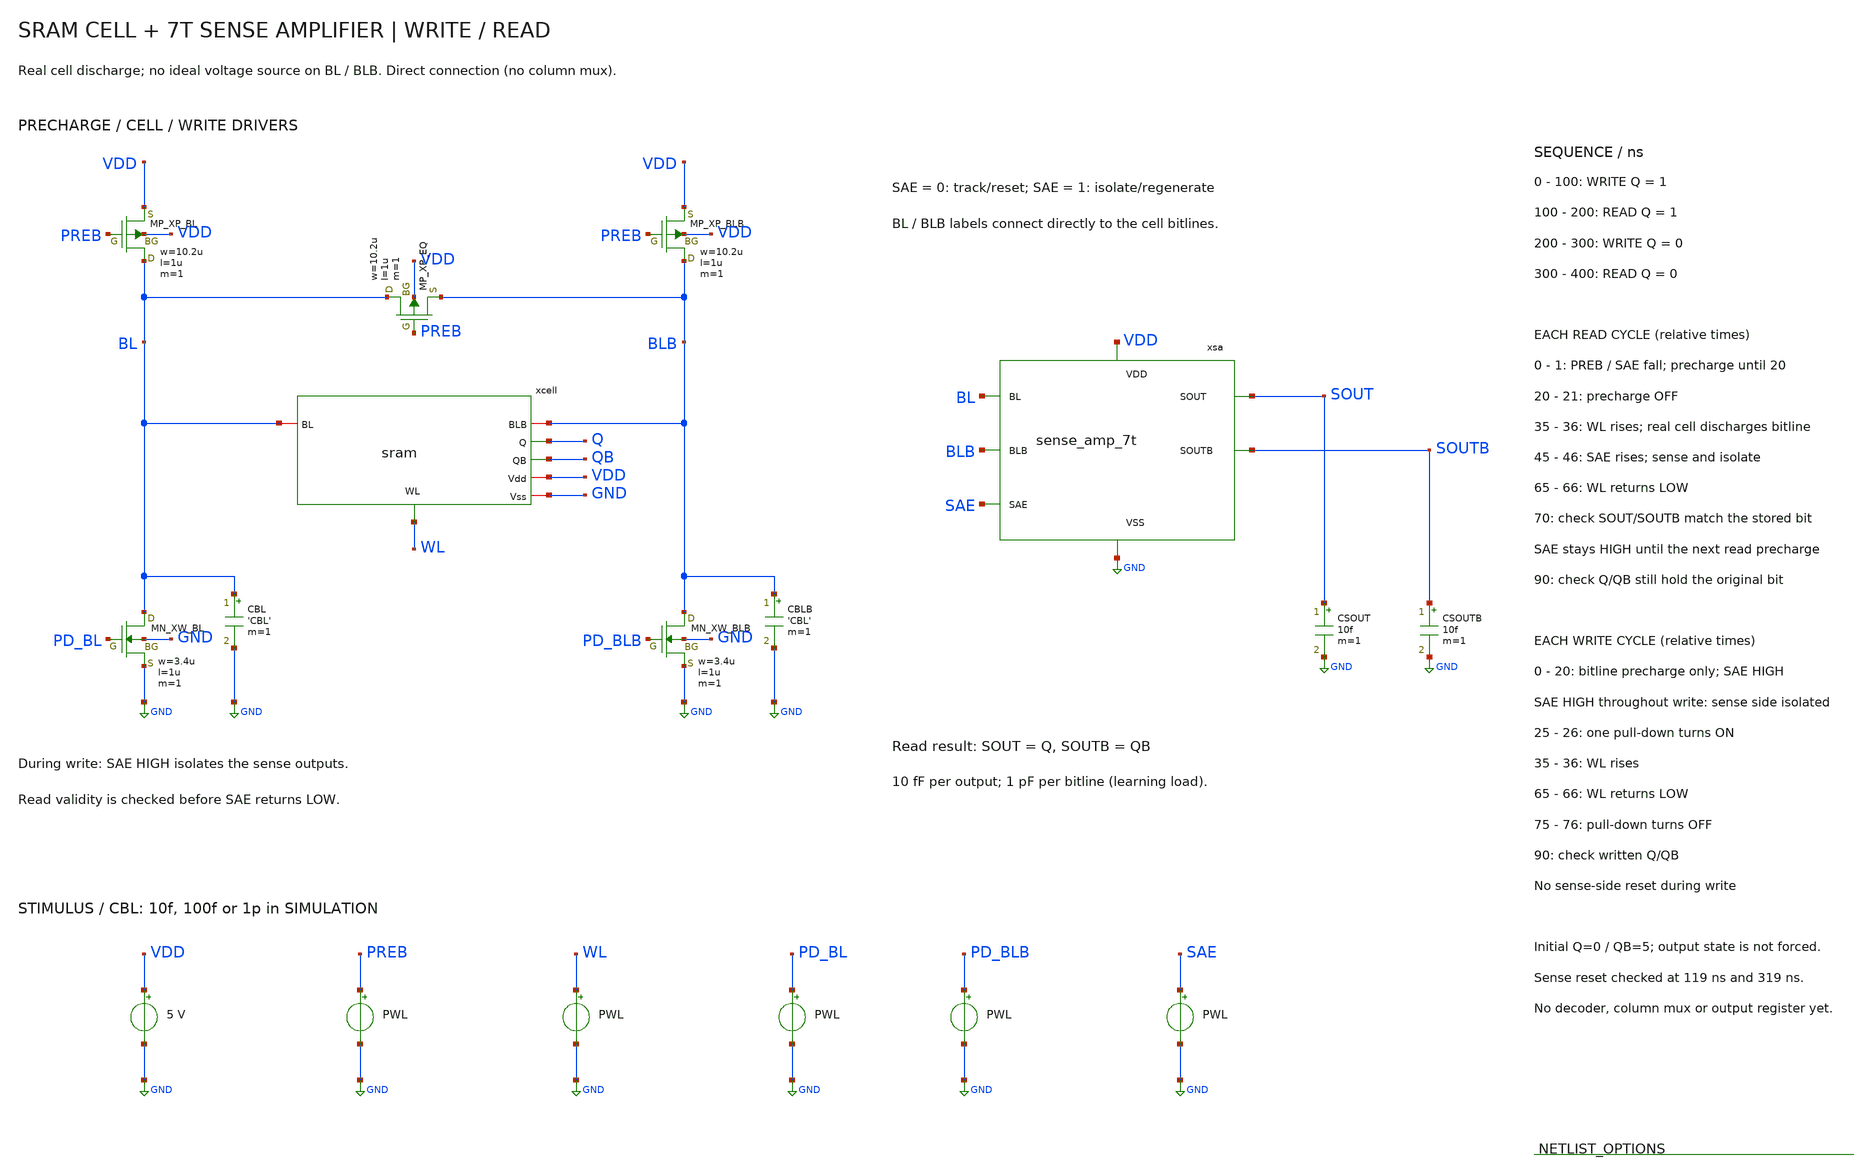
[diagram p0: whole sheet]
** sch_path: member_project/SRAM/PenguinEino/learning/schematics/sram_tb_cell_sense.sch
**.subckt sram_tb_cell_sense
XXP_BL BL PREB VDD VDD PMOS w=10.2u l=1u nrd=0 nrs=0 m=1
XXW_BL BL PD_BL GND GND NMOS w=3.4u l=1u nrd=0 nrs=0 m=1
XXP_BLB BLB PREB VDD VDD PMOS w=10.2u l=1u nrd=0 nrs=0 m=1
XXW_BLB BLB PD_BLB GND GND NMOS w=3.4u l=1u nrd=0 nrs=0 m=1
XXP_EQ BL PREB BLB VDD PMOS w=10.2u l=1u nrd=0 nrs=0 m=1
xcell WL VDD BLB Q QB BL GND sram
CBL BL GND 'CBL' m=1
CBLB BLB GND 'CBL' m=1
xsa BL BLB SAE SOUT SOUTB VDD GND sense_amp_7t
CSOUT SOUT GND 10f m=1
CSOUTB SOUTB GND 10f m=1
VVDD VDD GND 5
VPREB PREB GND PWL(0n 0 20n 0 21n 5 100n 5 101n 0 120n 0 121n 5 200n 5 201n 0 220n 0 221n 5 300n 5
+ 301n 0 320n 0 321n 5 400n 5)
VWL WL GND PWL(0n 0 35n 0 36n 5 65n 5 66n 0 135n 0 136n 5 165n 5 166n 0 235n 0 236n 5 265n 5 266n 0
+ 335n 0 336n 5 365n 5 366n 0 400n 0)
VPD_BL PD_BL GND PWL(0n 0 225n 0 226n 5 275n 5 276n 0 400n 0)
VPD_BLB PD_BLB GND PWL(0n 0 25n 0 26n 5 75n 5 76n 0 400n 0)
VSAE SAE GND PWL(0n 5 100n 5 101n 0 145n 0 146n 5 300n 5 301n 0 345n 0 346n 5 400n 5)
**** begin user architecture code
 .include $::LIB/ip62_models

.param CBL=1p
.ic v(Q)=0 v(QB)=5
.control
save all
tran 0.02n 400n
let failures = 0
let bl_diff = v(BL)-v(BLB)
meas tran q_hold_0 find v(Q) at=90n
meas tran qb_hold_0 find v(QB) at=90n
if q_hold_0 < 4.5 or qb_hold_0 > 0.5
 let failures = failures + 1
end
meas tran q_hold_1 find v(Q) at=190n
meas tran qb_hold_1 find v(QB) at=190n
if q_hold_1 < 4.5 or qb_hold_1 > 0.5
 let failures = failures + 1
end
meas tran reset_1 find v(SOUT) at=119n
meas tran resetb_1 find v(SOUTB) at=119n
if reset_1 < 4.5 or resetb_1 < 4.5
 let failures = failures + 1
end
meas tran read_1 find v(SOUT) at=170n
meas tran readb_1 find v(SOUTB) at=170n
if read_1 < 4.5 or readb_1 > 0.5
 let failures = failures + 1
end
meas tran input_diff_1 find bl_diff at=145n
meas tran low_node_peak_1 max v(QB) from=135n to=166n
meas tran q_hold_2 find v(Q) at=290n
meas tran qb_hold_2 find v(QB) at=290n
if q_hold_2 > 0.5 or qb_hold_2 < 4.5
 let failures = failures + 1
end
meas tran q_hold_3 find v(Q) at=390n
meas tran qb_hold_3 find v(QB) at=390n
if q_hold_3 > 0.5 or qb_hold_3 < 4.5
 let failures = failures + 1
end
meas tran reset_3 find v(SOUT) at=319n
meas tran resetb_3 find v(SOUTB) at=319n
if reset_3 < 4.5 or resetb_3 < 4.5
 let failures = failures + 1
end
meas tran read_3 find v(SOUT) at=370n
meas tran readb_3 find v(SOUTB) at=370n
if read_3 > 0.5 or readb_3 < 4.5
 let failures = failures + 1
end
meas tran input_diff_3 find bl_diff at=345n
meas tran low_node_peak_3 max v(Q) from=335n to=366n
if failures = 0
 echo PASS: real-cell writes, sensed reads, reset and cell retention
else
 echo FAIL: inspect writes, sense outputs and cell retention
 print failures
end
write sram_tb_cell_sense.raw
plot v(Q) v(QB) ylimit -0.5 5.5 title 'CELL: write 1 / read 1 / write 0 / read 0'
plot v(BL) v(BLB) title 'BITLINES: actual cell discharge and sense loading'
plot v(BL) v(BLB) v(SOUT) v(SOUTB) xlimit 130n 170n title 'READ 1 ZOOM: WL rises at 135 ns / SAE rises at 145 ns'
plot v(SOUT) v(SOUTB) title 'SENSE OUTPUTS: check at 170 ns and 370 ns'
let PREB_T = v(PREB)/5+8
let WL_T = v(WL)/5+6
let SAE_T = v(SAE)/5+4
let PD_BL_T = v(PD_BL)/5+2
let PD_BLB_T = v(PD_BLB)/5+0
plot PREB_T WL_T SAE_T PD_BL_T PD_BLB_T ylimit -0.3 9.3 title 'CONTROLS: PREB+8 / WL+6 / SAE+4 / PD_BL+2 / PD_BLB+0'
.endc

**** end user architecture code
**.ends
.GLOBAL GND
.end
